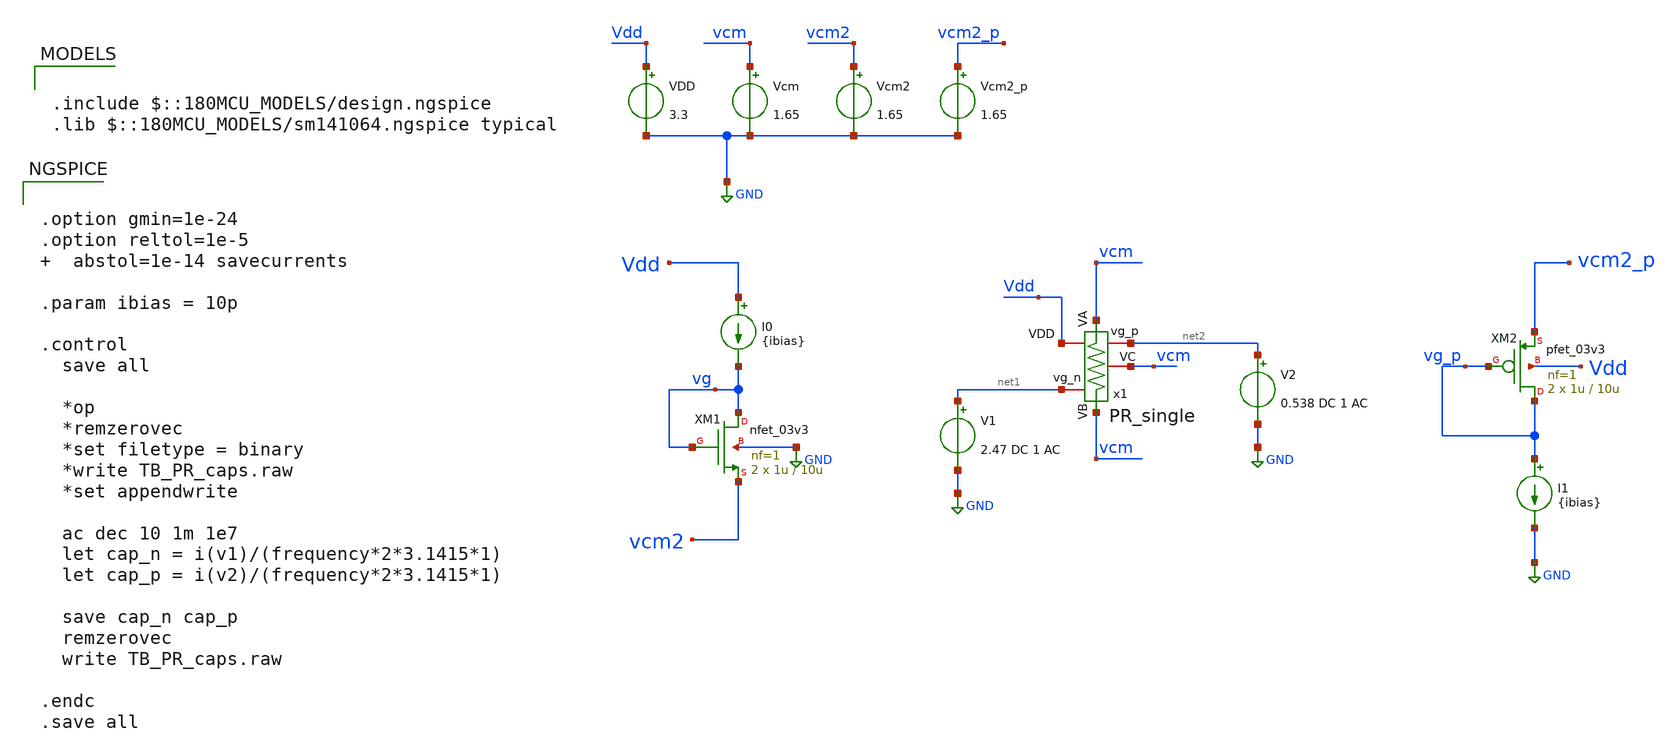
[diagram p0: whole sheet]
** sch_path: TIA/xschem/pseudo_res_dir/TB_PR_caps.sch
**.subckt TB_PR_caps
x1 Vdd vcm net2 vcm net1 vcm PR_single
I0 Vdd vg {ibias}
XM1 vg vg vcm2 GND nfet_03v3 L=10u W=1u nf=1 ad='int((nf+1)/2) * W/nf * 0.18u' as='int((nf+2)/2) * W/nf * 0.18u'
+ pd='2*int((nf+1)/2) * (W/nf + 0.18u)' ps='2*int((nf+2)/2) * (W/nf + 0.18u)' nrd='0.18u / W' nrs='0.18u / W'
+ sa=0 sb=0 sd=0 m=2
V1 net1 GND 2.47 DC 1 AC
V2 net2 GND 0.538 DC 1 AC
XM2 vg_p vg_p vcm2_p Vdd pfet_03v3 L=10u W=1u nf=1 ad='int((nf+1)/2) * W/nf * 0.18u' as='int((nf+2)/2) * W/nf * 0.18u'
+ pd='2*int((nf+1)/2) * (W/nf + 0.18u)' ps='2*int((nf+2)/2) * (W/nf + 0.18u)' nrd='0.18u / W' nrs='0.18u / W'
+ sa=0 sb=0 sd=0 m=2
I1 vg_p GND {ibias}
VDD Vdd GND 3.3
Vcm2 vcm2 GND 1.65
Vcm2_p vcm2_p GND 1.65
Vcm vcm GND 1.65
**** begin user architecture code

.include $::180MCU_MODELS/design.ngspice
.lib $::180MCU_MODELS/sm141064.ngspice typical



.option gmin=1e-24
.option reltol=1e-5   abstol=1e-14 savecurrents

.param ibias = 10p

.control
  save all

  *op
  *remzerovec
  *set filetype = binary
  *write TB_PR_caps.raw
  *set appendwrite

  ac dec 10 1m 1e7
  let cap_n = i(v1)/(frequency*2*3.1415*1)
  let cap_p = i(v2)/(frequency*2*3.1415*1)

  save cap_n cap_p
  remzerovec
  write TB_PR_caps.raw

.endc
.save all


**** end user architecture code
**.ends

* expanding   symbol:  /home/gmaranhao/Desktop/gf180_work/pseudo_res/PR_single.sym # of pins=6
** sym_path: TIA/xschem/pseudo_res_dir/PR_single.sym
** sch_path: TIA/xschem/pseudo_res_dir/PR_single.sch
.subckt PR_single VDD VA vg_p VC vg_n VB
*.iopin VB
*.iopin VA
*.iopin vg_n
*.iopin vg_p
*.iopin VC
*.iopin VDD
XM1 net1 vg_n VC GND nfet_03v3 L=10u W=1u nf=1 ad='int((nf+1)/2) * W/nf * 0.18u' as='int((nf+2)/2) * W/nf * 0.18u'
+ pd='2*int((nf+1)/2) * (W/nf + 0.18u)' ps='2*int((nf+2)/2) * (W/nf + 0.18u)' nrd='0.18u / W' nrs='0.18u / W'
+ sa=0 sb=0 sd=0 m=1
XM3 net1 vg_p VA VDD pfet_03v3 L=10u W=1u nf=1 ad='int((nf+1)/2) * W/nf * 0.18u' as='int((nf+2)/2) * W/nf * 0.18u'
+ pd='2*int((nf+1)/2) * (W/nf + 0.18u)' ps='2*int((nf+2)/2) * (W/nf + 0.18u)' nrd='0.18u / W' nrs='0.18u / W'
+ sa=0 sb=0 sd=0 m=1
XM2 net2 vg_n VC GND nfet_03v3 L=10u W=1u nf=1 ad='int((nf+1)/2) * W/nf * 0.18u' as='int((nf+2)/2) * W/nf * 0.18u'
+ pd='2*int((nf+1)/2) * (W/nf + 0.18u)' ps='2*int((nf+2)/2) * (W/nf + 0.18u)' nrd='0.18u / W' nrs='0.18u / W'
+ sa=0 sb=0 sd=0 m=1
XM4 net2 vg_p VB VDD pfet_03v3 L=10u W=1u nf=1 ad='int((nf+1)/2) * W/nf * 0.18u' as='int((nf+2)/2) * W/nf * 0.18u'
+ pd='2*int((nf+1)/2) * (W/nf + 0.18u)' ps='2*int((nf+2)/2) * (W/nf + 0.18u)' nrd='0.18u / W' nrs='0.18u / W'
+ sa=0 sb=0 sd=0 m=1
.ends

.GLOBAL GND
.end
